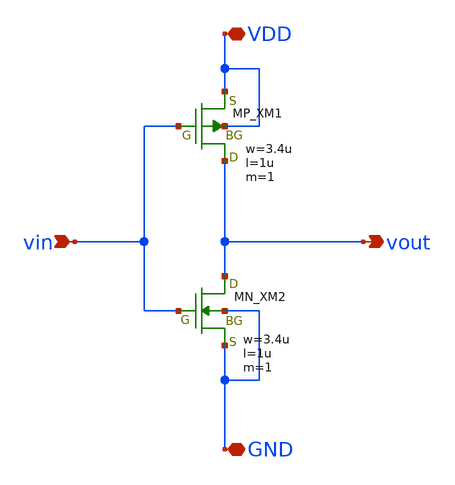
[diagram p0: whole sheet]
** sch_path: member_project/inverter/ichiken/ANT_taro/inverter_ANT_taro.sch
**.subckt inverter_ANT_taro VDD vin GND vout
*.iopin VDD
*.ipin vin
*.iopin GND
*.opin vout
XXM1 vout vin VDD VDD PMOS w=3.4u l=1u nrd=0 nrs=0 m=1
XXM2 vout vin GND GND NMOS w=3.4u l=1u nrd=0 nrs=0 m=1
**.ends
.end
